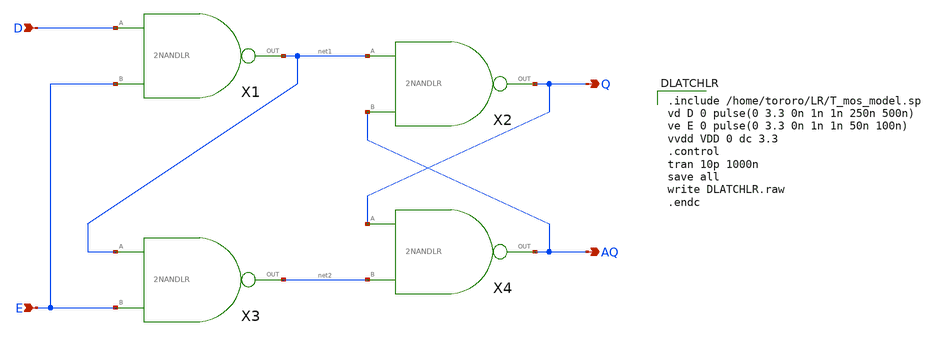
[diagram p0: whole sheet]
** sch_path: task_LATCH/DLATCHLR.sch
**.subckt DLATCHLR D E Q AQ
*.ipin D
*.ipin E
*.opin Q
*.opin AQ
X1 D E net1 2NANDLR
X2 net1 AQ Q 2NANDLR
X3 net1 E net2 2NANDLR
X4 Q net2 AQ 2NANDLR
**** begin user architecture code

.include /home/tororo/LR/T_mos_model.sp
vd D 0 pulse(0 3.3 0n 1n 1n 250n 500n)
ve E 0 pulse(0 3.3 0n 1n 1n 50n 100n)
vvdd VDD 0 dc 3.3
.control
tran 10p 1000n
save all
write DLATCHLR.raw
.endc

**** end user architecture code
**.ends

* expanding   symbol:  LR/task_LATCH/2NANDLR.sym # of pins=3
** sym_path: task_LATCH/2NANDLR.sym
** sch_path: task_LATCH/2NANDLR.sch
.subckt 2NANDLR A B OUT
*.ipin A
*.ipin B
*.opin OUT
M1 OUT A net1 GND nch w=3.5u l=3.5u as=0 ps=0 ad=0 pd=0 m=1
M2 OUT B VDD VDD pch w=10.5u l=3.5u as=0 ps=0 ad=0 pd=0 m=1
M3 OUT A VDD VDD pch w=10.5u l=3.5u as=0 ps=0 ad=0 pd=0 m=1
M4 net1 B GND GND nch w=3.5u l=10.5u as=0 ps=0 ad=0 pd=0 m=1
.ends

.GLOBAL VDD
.GLOBAL GND
.end
